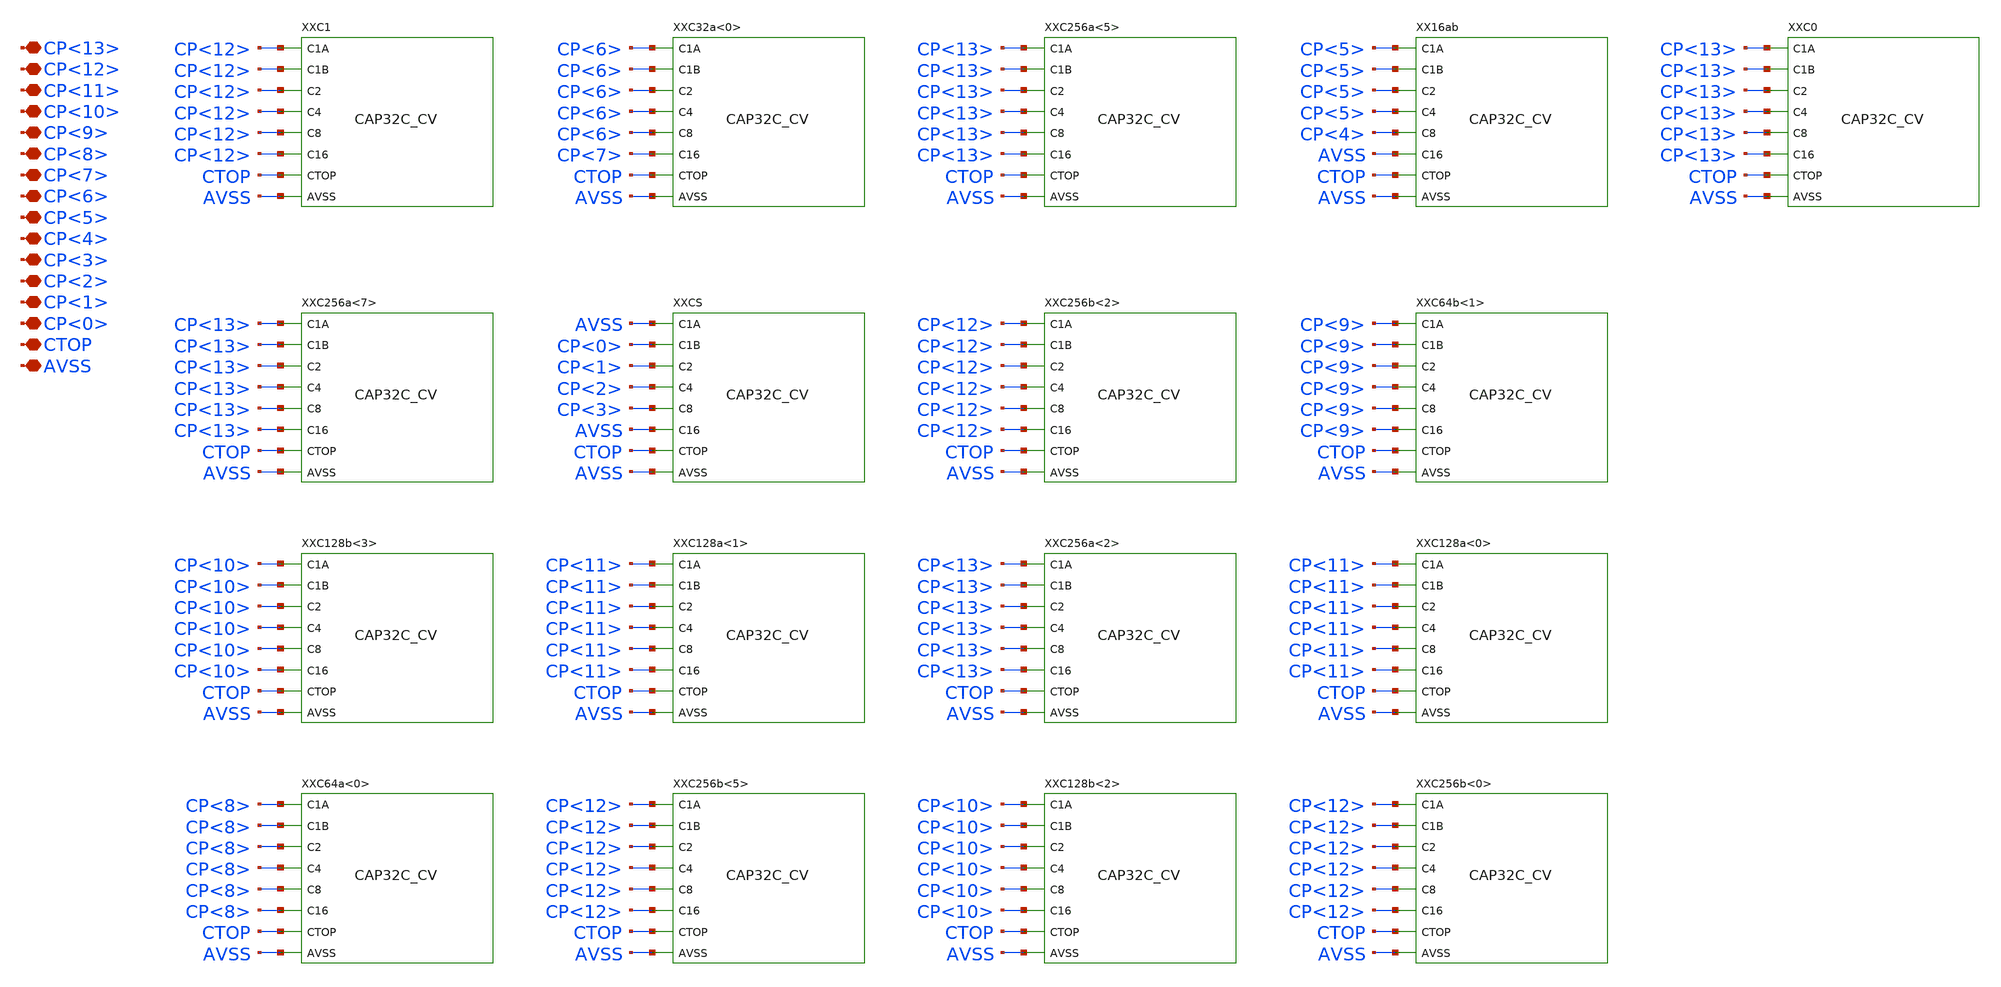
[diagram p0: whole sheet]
** sch_path: tests/transpile/SAR9B/CDAC9_CV.sch
**.subckt CDAC9_CV CP<13> CP<12> CP<11> CP<10> CP<9> CP<8> CP<7> CP<6> CP<5> CP<4> CP<3> CP<2> CP<1>
*+ CP<0> CTOP AVSS
*.iopin CP<13>
*.iopin CP<12>
*.iopin CP<11>
*.iopin CP<10>
*.iopin CP<9>
*.iopin CP<8>
*.iopin CP<7>
*.iopin CP<6>
*.iopin CP<5>
*.iopin CP<4>
*.iopin CP<3>
*.iopin CP<2>
*.iopin CP<1>
*.iopin CP<0>
*.iopin CTOP
*.iopin AVSS
XXC1 CP<12> CP<12> CP<12> CP<12> CP<12> CP<12> CTOP AVSS CAP32C_CV
XXC256a<7> CP<13> CP<13> CP<13> CP<13> CP<13> CP<13> CTOP AVSS CAP32C_CV
XXC128b<3> CP<10> CP<10> CP<10> CP<10> CP<10> CP<10> CTOP AVSS CAP32C_CV
XXC64a<0> CP<8> CP<8> CP<8> CP<8> CP<8> CP<8> CTOP AVSS CAP32C_CV
XXC32a<0> CP<6> CP<6> CP<6> CP<6> CP<6> CP<7> CTOP AVSS CAP32C_CV
XXCS AVSS CP<0> CP<1> CP<2> CP<3> AVSS CTOP AVSS CAP32C_CV
XXC128a<1> CP<11> CP<11> CP<11> CP<11> CP<11> CP<11> CTOP AVSS CAP32C_CV
XXC256b<5> CP<12> CP<12> CP<12> CP<12> CP<12> CP<12> CTOP AVSS CAP32C_CV
XXC256a<5> CP<13> CP<13> CP<13> CP<13> CP<13> CP<13> CTOP AVSS CAP32C_CV
XXC256b<2> CP<12> CP<12> CP<12> CP<12> CP<12> CP<12> CTOP AVSS CAP32C_CV
XXC256a<2> CP<13> CP<13> CP<13> CP<13> CP<13> CP<13> CTOP AVSS CAP32C_CV
XXC128b<2> CP<10> CP<10> CP<10> CP<10> CP<10> CP<10> CTOP AVSS CAP32C_CV
XX16ab CP<5> CP<5> CP<5> CP<5> CP<4> AVSS CTOP AVSS CAP32C_CV
XXC64b<1> CP<9> CP<9> CP<9> CP<9> CP<9> CP<9> CTOP AVSS CAP32C_CV
XXC128a<0> CP<11> CP<11> CP<11> CP<11> CP<11> CP<11> CTOP AVSS CAP32C_CV
XXC256b<0> CP<12> CP<12> CP<12> CP<12> CP<12> CP<12> CTOP AVSS CAP32C_CV
XXC0 CP<13> CP<13> CP<13> CP<13> CP<13> CP<13> CTOP AVSS CAP32C_CV
**.ends

* expanding   symbol:  SAR9B/CAP32C_CV.sym # of pins=8
** sym_path: tests/transpile/SAR9B/CAP32C_CV.sym
** sch_path: tests/transpile/SAR9B/CAP32C_CV.sch
.subckt CAP32C_CV C1A C1B C2 C4 C8 C16 CTOP AVSS
*.iopin C1A
*.iopin C1B
*.iopin C2
*.iopin C4
*.iopin C8
*.iopin C16
*.iopin CTOP
*.iopin AVSS
XXRES1A C1A NC1 RM1
XXRES1B C1B NC2 RM1
XXRES2 C2 NC3 RM1
XXRES4 C4 NC4 RM1
XXRES8 C8 NC5 RM1
XXRES16 C16 NC6 RM1
.ends


* expanding   symbol:  SAR9B/RM1.sym # of pins=2
** sym_path: tests/transpile/SAR9B/RM1.sym
** sch_path: tests/transpile/SAR9B/RM1.sch
.subckt RM1 A B
*.iopin A
*.iopin B
R1 A B (value) m=1
.ends

.end
